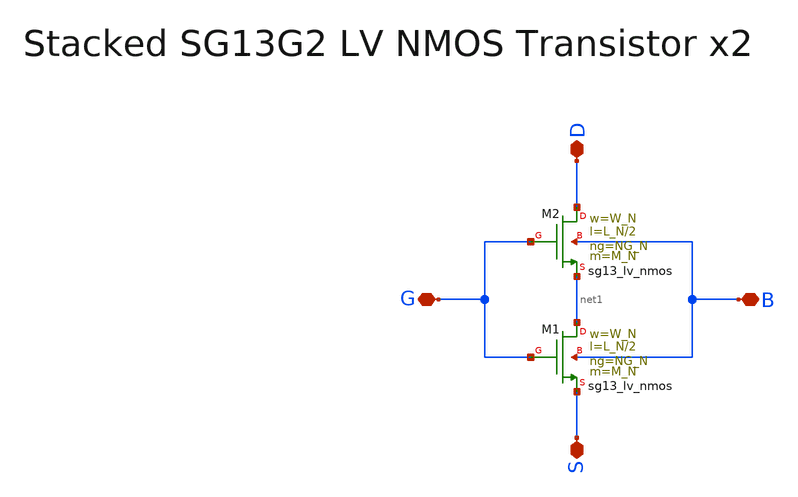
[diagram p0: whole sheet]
** sch_path: SG13G2_ATBS-ADC-main/xschem/stacked_transistors/sg13g2_lv_nmos_stacked/sg13g2_lv_nmos_stacked_x2.sch
**.subckt sg13g2_lv_nmos_stacked_x2 D S G B
*.iopin D
*.iopin S
*.iopin G
*.iopin B
XM1 net1 G S B sg13_lv_nmos w=W_N l=L_N/2 ng=NG_N m=M_N mm_ok=1
XM2 D G net1 B sg13_lv_nmos w=W_N l=L_N/2 ng=NG_N m=M_N mm_ok=1
**.ends
.end
